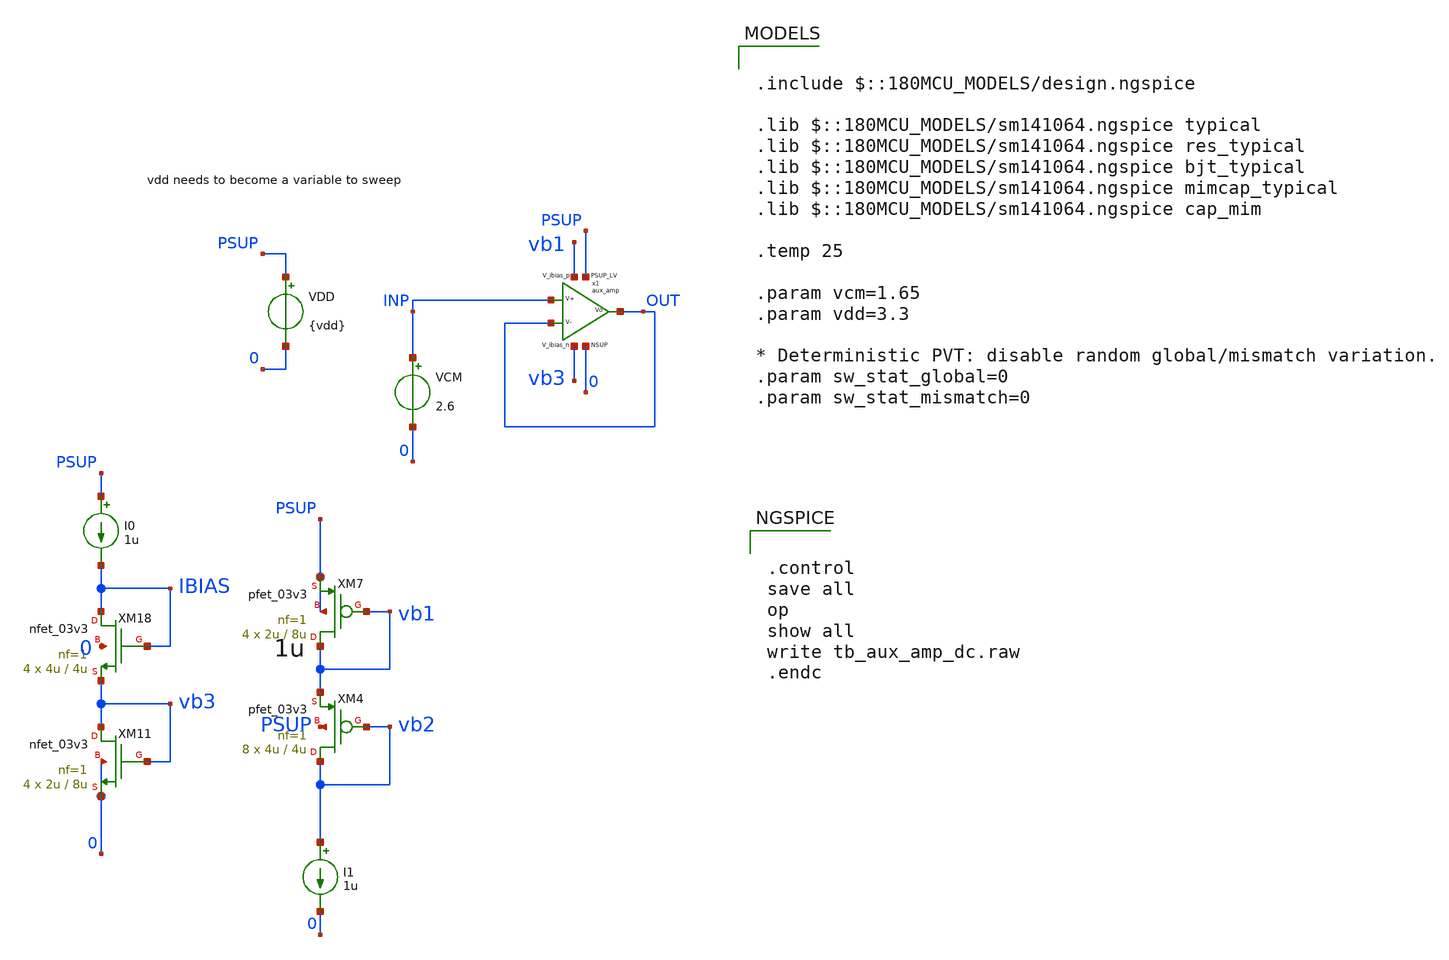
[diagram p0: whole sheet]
** sch_path: xschem/blocks/aux_amp/tb_aux_amp_dc.sch
**.subckt tb_aux_amp_dc
VDD PSUP 0 {vdd}
VCM INP 0 2.6
x1 PSUP OUT INP OUT vb3 0 vb1 aux_amp
XM11 vb3 vb3 0 0 nfet_03v3 L=8u W=2u nf=1 ad='int((nf+1)/2) * W/nf * 0.18u' as='int((nf+2)/2) * W/nf * 0.18u'
+ pd='2*int((nf+1)/2) * (W/nf + 0.18u)' ps='2*int((nf+2)/2) * (W/nf + 0.18u)' nrd='0.18u / W' nrs='0.18u / W'
+ sa=0 sb=0 sd=0 m=4
XM18 IBIAS IBIAS vb3 0 nfet_03v3 L=4u W=4u nf=1 ad='int((nf+1)/2) * W/nf * 0.18u' as='int((nf+2)/2) * W/nf * 0.18u'
+ pd='2*int((nf+1)/2) * (W/nf + 0.18u)' ps='2*int((nf+2)/2) * (W/nf + 0.18u)' nrd='0.18u / W' nrs='0.18u / W'
+ sa=0 sb=0 sd=0 m=4
I0 PSUP IBIAS 1u
XM7 vb1 vb1 PSUP PSUP pfet_03v3 L=8u W=2u nf=1 ad='int((nf+1)/2) * W/nf * 0.18u' as='int((nf+2)/2) * W/nf * 0.18u'
+ pd='2*int((nf+1)/2) * (W/nf + 0.18u)' ps='2*int((nf+2)/2) * (W/nf + 0.18u)' nrd='0.18u / W' nrs='0.18u / W'
+ sa=0 sb=0 sd=0 m=4
XM4 vb2 vb2 vb1 PSUP pfet_03v3 L=4u W=4u nf=1 ad='int((nf+1)/2) * W/nf * 0.18u' as='int((nf+2)/2) * W/nf * 0.18u'
+ pd='2*int((nf+1)/2) * (W/nf + 0.18u)' ps='2*int((nf+2)/2) * (W/nf + 0.18u)' nrd='0.18u / W' nrs='0.18u / W'
+ sa=0 sb=0 sd=0 m=8
I1 vb2 0 1u
**** begin user architecture code


.control
save all
op
show all
write tb_aux_amp_dc.raw
.endc



.include $::180MCU_MODELS/design.ngspice

.lib $::180MCU_MODELS/sm141064.ngspice typical
.lib $::180MCU_MODELS/sm141064.ngspice res_typical
.lib $::180MCU_MODELS/sm141064.ngspice bjt_typical
.lib $::180MCU_MODELS/sm141064.ngspice mimcap_typical
.lib $::180MCU_MODELS/sm141064.ngspice cap_mim

.temp 25

.param vcm=1.65
.param vdd=3.3

* Deterministic PVT: disable random global/mismatch variation.
.param sw_stat_global=0
.param sw_stat_mismatch=0


**** end user architecture code
**.ends
.end
